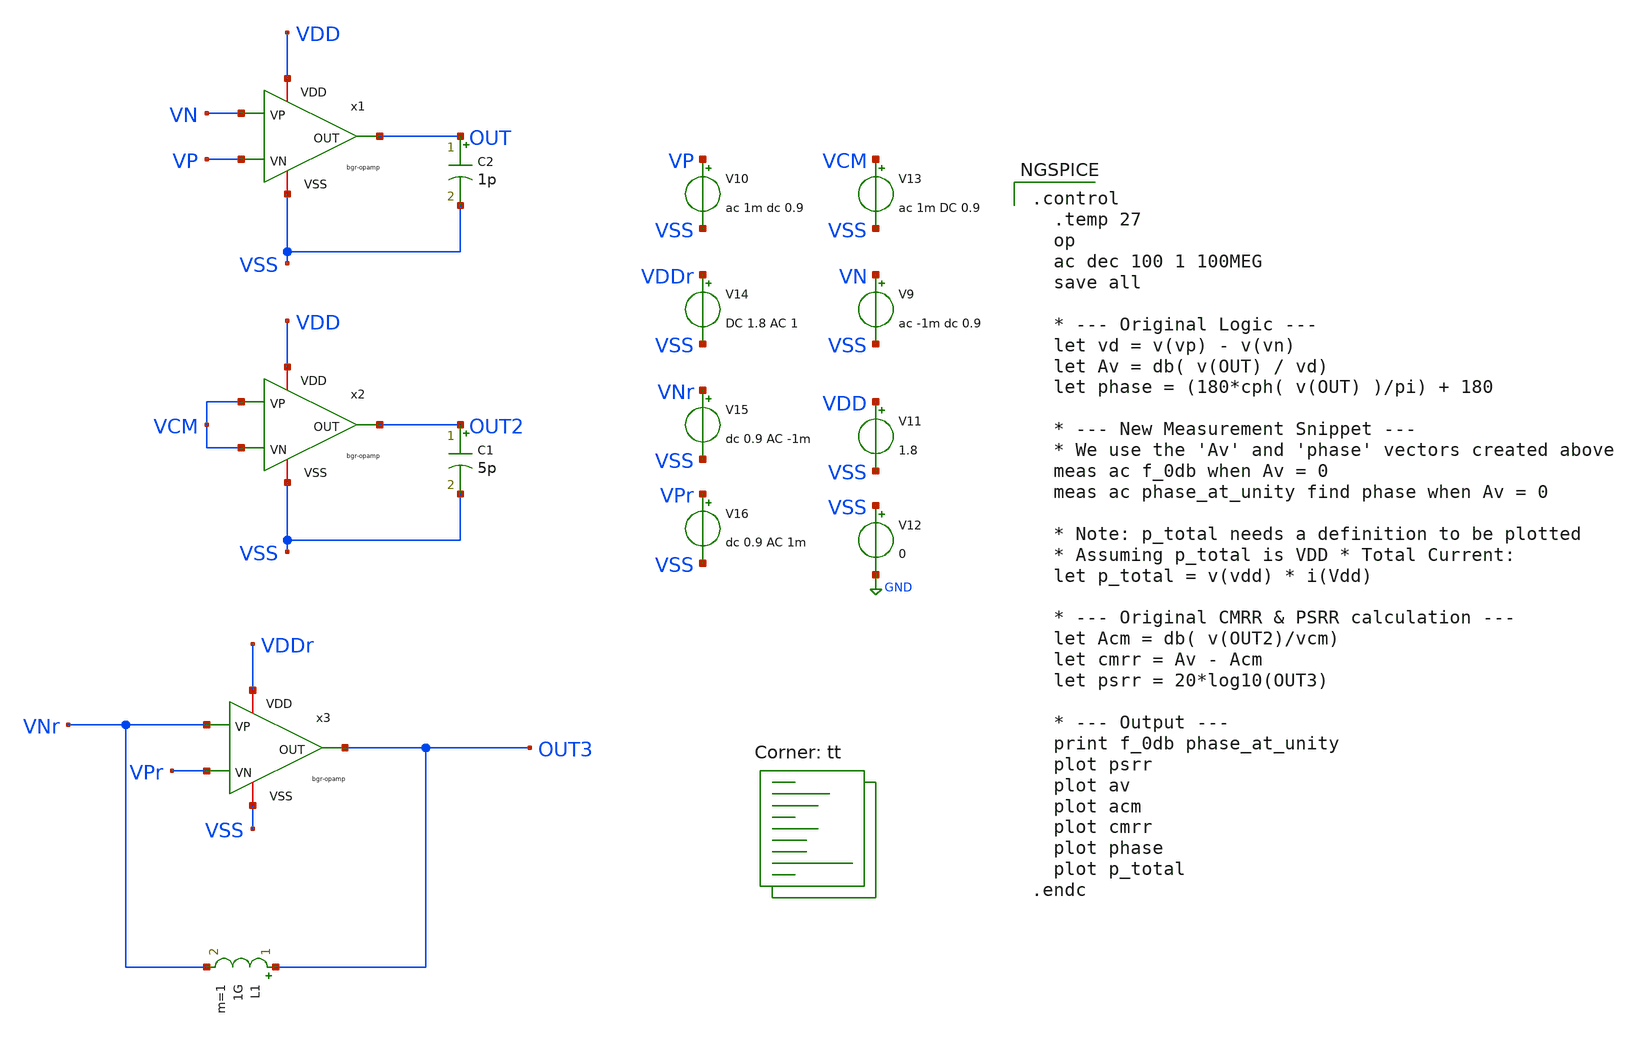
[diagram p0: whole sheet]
** sch_path: bandgap/bgr-opamp/tb_ac.sch
**.subckt tb_ac
C2 OUT VSS 1p m=1
C1 OUT2 VSS 5p m=1
x1 VDD OUT VN VP VSS bgr-opamp
x2 VDD OUT2 VCM VCM VSS bgr-opamp
x3 VDDr OUT3 VNr VPr VSS bgr-opamp
L1 OUT3 VNr 1G m=1
V9 VN VSS ac -1m dc 0.9
V10 VP VSS ac 1m dc 0.9
V11 VDD VSS 1.8
V12 VSS GND 0
V13 VCM VSS ac 1m DC 0.9
V14 VDDr VSS DC 1.8 AC 1
V15 VNr VSS dc 0.9 AC -1m
V16 VPr VSS dc 0.9 AC 1m
**** begin user architecture code

.control
  .temp 27
  op
  ac dec 100 1 100MEG
  save all

  * --- Original Logic ---
  let vd = v(vp) - v(vn)
  let Av = db( v(OUT) / vd)
  let phase = (180*cph( v(OUT) )/pi) + 180

  * --- New Measurement Snippet ---
  * We use the 'Av' and 'phase' vectors created above
  meas ac f_0db when Av = 0
  meas ac phase_at_unity find phase when Av = 0

  * Note: p_total needs a definition to be plotted
  * Assuming p_total is VDD * Total Current:
  let p_total = v(vdd) * i(Vdd)

  * --- Original CMRR & PSRR calculation ---
  let Acm = db( v(OUT2)/vcm)
  let cmrr = Av - Acm
  let psrr = 20*log10(OUT3)

  * --- Output ---
  print f_0db phase_at_unity
  plot psrr
  plot av
  plot acm
  plot cmrr
  plot phase
  plot p_total
.endc



.lib $::SKYWATER_MODELS/sky130.lib.spice tt
**** end user architecture code
**.ends

* expanding   symbol:  afe-icdec-teknofest-2026/bandgap/bgr-opamp/bgr-opamp.sym # of pins=5
** sym_path: bandgap/bgr-opamp/bgr-opamp.sym
** sch_path: bandgap/bgr-opamp/bgr-opamp.sch
.subckt bgr-opamp VDD OUT VP VN VSS
*.iopin VSS
*.iopin VDD
*.ipin VP
*.ipin VN
*.opin OUT
XM1 net1 VP net3 VSS sky130_fd_pr__nfet_01v8 L=0.3 W=2.5 nf=2 ad='int((nf+1)/2) * W/nf * 0.29' as='int((nf+2)/2) * W/nf * 0.29'
+ pd='2*int((nf+1)/2) * (W/nf + 0.29)' ps='2*int((nf+2)/2) * (W/nf + 0.29)' nrd='0.29 / W' nrs='0.29 / W'
+ sa=0 sb=0 sd=0 mult=1 m=1
XM2 net2 VN net3 VSS sky130_fd_pr__nfet_01v8 L=0.3 W=2.5 nf=2 ad='int((nf+1)/2) * W/nf * 0.29' as='int((nf+2)/2) * W/nf * 0.29'
+ pd='2*int((nf+1)/2) * (W/nf + 0.29)' ps='2*int((nf+2)/2) * (W/nf + 0.29)' nrd='0.29 / W' nrs='0.29 / W'
+ sa=0 sb=0 sd=0 mult=1 m=1
XM4 net2 net1 VDD VDD sky130_fd_pr__pfet_01v8 L=1.25 W=10.8 nf=4 ad='int((nf+1)/2) * W/nf * 0.29' as='int((nf+2)/2) * W/nf * 0.29'
+ pd='2*int((nf+1)/2) * (W/nf + 0.29)' ps='2*int((nf+2)/2) * (W/nf + 0.29)' nrd='0.29 / W' nrs='0.29 / W'
+ sa=0 sb=0 sd=0 mult=1 m=1
XM3 net1 net1 VDD VDD sky130_fd_pr__pfet_01v8 L=1.25 W=10.8 nf=4 ad='int((nf+1)/2) * W/nf * 0.29' as='int((nf+2)/2) * W/nf * 0.29'
+ pd='2*int((nf+1)/2) * (W/nf + 0.29)' ps='2*int((nf+2)/2) * (W/nf + 0.29)' nrd='0.29 / W' nrs='0.29 / W'
+ sa=0 sb=0 sd=0 mult=1 m=1
XM5 net3 net4 VSS VSS sky130_fd_pr__nfet_01v8 L=1.25 W=3.4 nf=1 ad='int((nf+1)/2) * W/nf * 0.29' as='int((nf+2)/2) * W/nf * 0.29'
+ pd='2*int((nf+1)/2) * (W/nf + 0.29)' ps='2*int((nf+2)/2) * (W/nf + 0.29)' nrd='0.29 / W' nrs='0.29 / W'
+ sa=0 sb=0 sd=0 mult=1 m=1
XM9 net4 net5 net10 VSS sky130_fd_pr__nfet_01v8 L=1.25 W=3.4 nf=1 ad='int((nf+1)/2) * W/nf * 0.29' as='int((nf+2)/2) * W/nf * 0.29'
+ pd='2*int((nf+1)/2) * (W/nf + 0.29)' ps='2*int((nf+2)/2) * (W/nf + 0.29)' nrd='0.29 / W' nrs='0.29 / W'
+ sa=0 sb=0 sd=0 mult=1 m=1
XM8 net4 net4 VDD VDD sky130_fd_pr__pfet_01v8 L=1.25 W=10.8 nf=4 ad='int((nf+1)/2) * W/nf * 0.29' as='int((nf+2)/2) * W/nf * 0.29'
+ pd='2*int((nf+1)/2) * (W/nf + 0.29)' ps='2*int((nf+2)/2) * (W/nf + 0.29)' nrd='0.29 / W' nrs='0.29 / W'
+ sa=0 sb=0 sd=0 mult=1 m=1
XM11 net5 net4 VDD VDD sky130_fd_pr__pfet_01v8 L=1.25 W=10.8 nf=4 ad='int((nf+1)/2) * W/nf * 0.29' as='int((nf+2)/2) * W/nf * 0.29'
+ pd='2*int((nf+1)/2) * (W/nf + 0.29)' ps='2*int((nf+2)/2) * (W/nf + 0.29)' nrd='0.29 / W' nrs='0.29 / W'
+ sa=0 sb=0 sd=0 mult=1 m=1
XM10 net5 net5 VSS VSS sky130_fd_pr__nfet_01v8 L=1.25 W=3.4 nf=1 ad='int((nf+1)/2) * W/nf * 0.29' as='int((nf+2)/2) * W/nf * 0.29'
+ pd='2*int((nf+1)/2) * (W/nf + 0.29)' ps='2*int((nf+2)/2) * (W/nf + 0.29)' nrd='0.29 / W' nrs='0.29 / W'
+ sa=0 sb=0 sd=0 mult=1 m=1
XM6 OUT net2 VDD VDD sky130_fd_pr__pfet_01v8 L=1.25 W=110 nf=32 ad='int((nf+1)/2) * W/nf * 0.29' as='int((nf+2)/2) * W/nf * 0.29'
+ pd='2*int((nf+1)/2) * (W/nf + 0.29)' ps='2*int((nf+2)/2) * (W/nf + 0.29)' nrd='0.29 / W' nrs='0.29 / W'
+ sa=0 sb=0 sd=0 mult=1 m=1
XM7 OUT net4 VSS VSS sky130_fd_pr__nfet_01v8 L=1.25 W=12 nf=4 ad='int((nf+1)/2) * W/nf * 0.29' as='int((nf+2)/2) * W/nf * 0.29'
+ pd='2*int((nf+1)/2) * (W/nf + 0.29)' ps='2*int((nf+2)/2) * (W/nf + 0.29)' nrd='0.29 / W' nrs='0.29 / W'
+ sa=0 sb=0 sd=0 mult=1 m=1
XC2 OUT net2 sky130_fd_pr__cap_mim_m3_1 W=15 L=15 MF=4 m=4
XM12 net4 net4 net5 VSS sky130_fd_pr__nfet_01v8 L=0.15 W=0.85 nf=1 ad='int((nf+1)/2) * W/nf * 0.29' as='int((nf+2)/2) * W/nf * 0.29'
+ pd='2*int((nf+1)/2) * (W/nf + 0.29)' ps='2*int((nf+2)/2) * (W/nf + 0.29)' nrd='0.29 / W' nrs='0.29 / W'
+ sa=0 sb=0 sd=0 mult=1 m=1
XR2 net6 net10 VSS sky130_fd_pr__res_high_po_1p41 L=3.235 mult=1 m=1
XR3 net8 net6 VSS sky130_fd_pr__res_high_po_1p41 L=3.235 mult=1 m=1
XR4 net7 net8 VSS sky130_fd_pr__res_high_po_1p41 L=3.235 mult=1 m=1
XR5 net9 net7 VSS sky130_fd_pr__res_high_po_1p41 L=3.235 mult=1 m=1
XR6 VSS net9 VSS sky130_fd_pr__res_high_po_1p41 L=3.235 mult=1 m=1
.ends

.GLOBAL GND
.end
